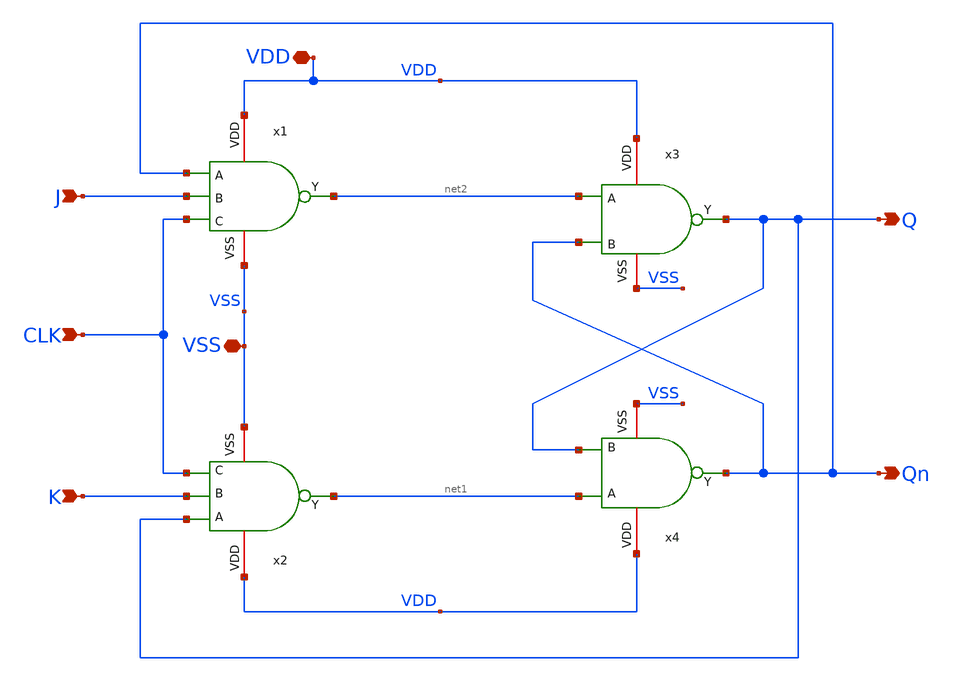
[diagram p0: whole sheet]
** sch_path: src/UN_PFD_GF180mcuD/UN_JKFF_GF180mcuD.sch
**.subckt UN_JKFF_GF180mcuD J CLK K Q Qn VDD VSS
*.ipin J
*.ipin CLK
*.ipin K
*.opin Q
*.opin Qn
*.iopin VDD
*.iopin VSS
x1 VDD net2 Qn J VSS CLK UN_NAND3_GF180mcuD
x2 VDD net1 Q K VSS CLK UN_NAND3_GF180mcuD
x3 VDD Q net2 Qn VSS UN_NAND2_GF180mcuD
x4 VDD Qn net1 Q VSS UN_NAND2_GF180mcuD
**.ends
.end
